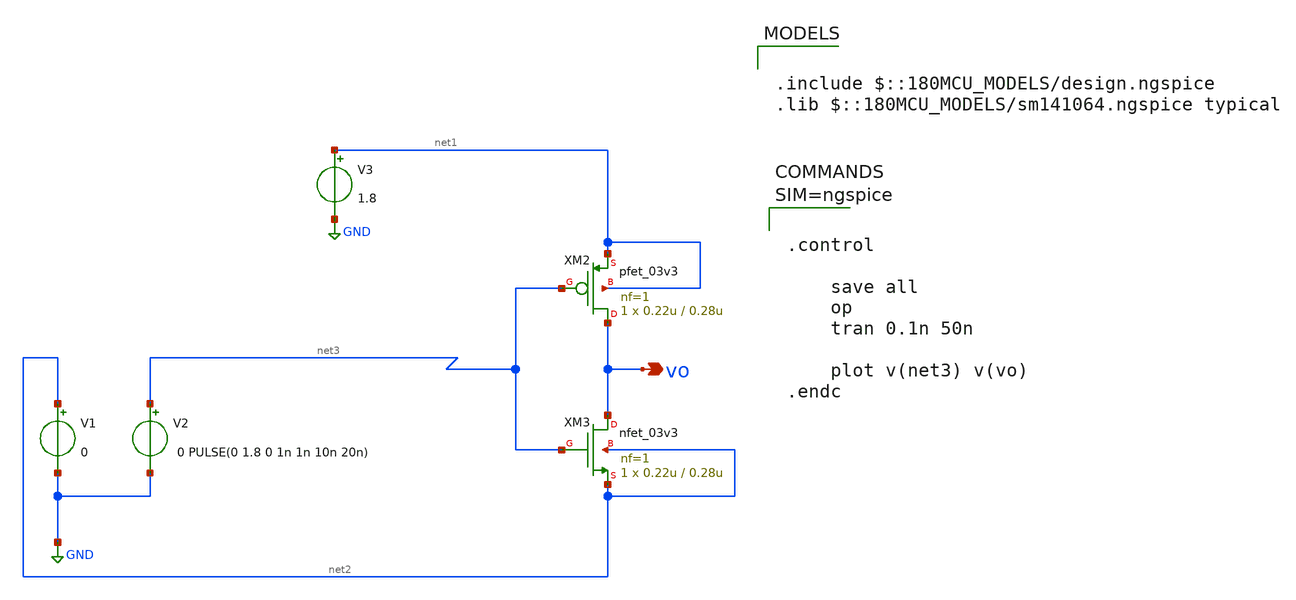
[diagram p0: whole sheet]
** sch_path: xschem/inv.sch
**.subckt inv vo
*.opin vo
XM3 vo net3 net2 net2 nfet_03v3 L=0.28u W=0.22u nf=1 ad='int((nf+1)/2) * W/nf * 0.18u' as='int((nf+2)/2) * W/nf * 0.18u'
+ pd='2*int((nf+1)/2) * (W/nf + 0.18u)' ps='2*int((nf+2)/2) * (W/nf + 0.18u)' nrd='0.18u / W' nrs='0.18u / W'
+ sa=0 sb=0 sd=0 m=1
XM2 vo net3 net1 net1 pfet_03v3 L=0.28u W=0.22u nf=1 ad='int((nf+1)/2) * W/nf * 0.18u' as='int((nf+2)/2) * W/nf * 0.18u'
+ pd='2*int((nf+1)/2) * (W/nf + 0.18u)' ps='2*int((nf+2)/2) * (W/nf + 0.18u)' nrd='0.18u / W' nrs='0.18u / W'
+ sa=0 sb=0 sd=0 m=1
V1 net2 GND 0
V2 net3 GND 0 PULSE(0 1.8 0 1n 1n 10n 20n)
V3 net1 GND 1.8
**** begin user architecture code



.control

    save all
    op
    tran 0.1n 50n

    plot v(net3) v(vo)
.endc





.include $::180MCU_MODELS/design.ngspice
.lib $::180MCU_MODELS/sm141064.ngspice typical

**** end user architecture code
**.ends
.GLOBAL GND
.end
